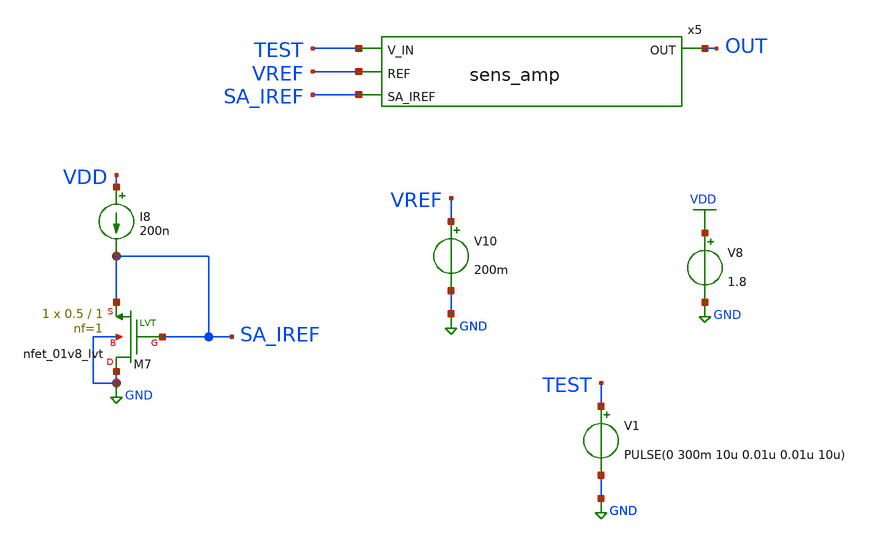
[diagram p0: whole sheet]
** sch_path: xschem/testbench/sens_amp_tb.sch
**.subckt sens_amp_tb
x5 OUT VREF TEST SA_IREF sens_amp
I8 VDD SA_IREF 200n
XM7 GND SA_IREF SA_IREF GND sky130_fd_pr__nfet_01v8_lvt L=1 W=0.5 nf=1 ad='int((nf+1)/2) * W/nf * 0.29'
+ as='int((nf+2)/2) * W/nf * 0.29' pd='2*int((nf+1)/2) * (W/nf + 0.29)' ps='2*int((nf+2)/2) * (W/nf + 0.29)'
+ nrd='0.29 / W' nrs='0.29 / W' sa=0 sb=0 sd=0 mult=1 m=1
V10 VREF GND 200m
V8 VDD GND 1.8
V1 TEST GND PULSE(0 300m 10u 0.01u 0.01u 10u)
**** begin user architecture code

** opencircuitdesign pdks install
.lib $::SKYWATER_MODELS/sky130.lib.spice tt


**** end user architecture code
**.ends

* expanding   symbol:  sens_amp.sym # of pins=4
** sym_path: xschem/sens_amp.sym
** sch_path: xschem/sens_amp.sch
.subckt sens_amp OUT REF V_IN SA_IREF
*.ipin REF
*.ipin V_IN
*.opin OUT
*.ipin SA_IREF
XM5 net1 GN VDD VDD sky130_fd_pr__pfet_01v8_lvt L=0.5 W=1 nf=1 ad='W * 0.29' as='W * 0.29' pd='2*(W + 0.29)'
+ ps='2*(W + 0.29)' nrd=0 nrs=0 sa=0 sb=0 sd=0 mult=1 m=1
XM6 GN GN VDD VDD sky130_fd_pr__pfet_01v8_lvt L=0.5 W=1 nf=1 ad='W * 0.29' as='W * 0.29' pd='2*(W + 0.29)'
+ ps='2*(W + 0.29)' nrd=0 nrs=0 sa=0 sb=0 sd=0 mult=1 m=1
XM23 net1 V_IN net2 GND sky130_fd_pr__nfet_01v8_lvt L=0.15 W=4 nf=1 ad='W * 0.29' as='W * 0.29' pd='2*(W + 0.29)'
+ ps='2*(W + 0.29)' nrd=0 nrs=0 sa=0 sb=0 sd=0 mult=1 m=1
XM16 GN REF net2 GND sky130_fd_pr__nfet_01v8_lvt L=0.15 W=4 nf=1 ad='W * 0.29' as='W * 0.29' pd='2*(W + 0.29)'
+ ps='2*(W + 0.29)' nrd=0 nrs=0 sa=0 sb=0 sd=0 mult=1 m=1
XM1 OUT net1 GND GND sky130_fd_pr__nfet_01v8_lvt L=0.15 W=1 nf=1 ad='W * 0.29' as='W * 0.29' pd='2*(W + 0.29)'
+ ps='2*(W + 0.29)' nrd=0 nrs=0 sa=0 sb=0 sd=0 mult=1 m=1
XM2 OUT net1 VDD VDD sky130_fd_pr__pfet_01v8_lvt L=0.35 W=3 nf=1 ad='W * 0.29' as='W * 0.29' pd='2*(W + 0.29)'
+ ps='2*(W + 0.29)' nrd=0 nrs=0 sa=0 sb=0 sd=0 mult=1 m=1
XM3 net3 SA_IREF GND GND sky130_fd_pr__nfet_01v8_lvt L=1 W=0.5 nf=1 ad='W * 0.29' as='W * 0.29' pd='2*(W + 0.29)'
+ ps='2*(W + 0.29)' nrd=0 nrs=0 sa=0 sb=0 sd=0 mult=1 m=1
Vmeas net2 net3 0
.save i(vmeas)
.ends

.GLOBAL GND
.GLOBAL VDD
**** begin user architecture code


.options gmin=10e-20
.control
save all

*dc v2 0 1.8 0.05
*plot v(test)
tran 1u 200u

write sim_dpspixel_tb.raw
.endc


**** end user architecture code
.end
